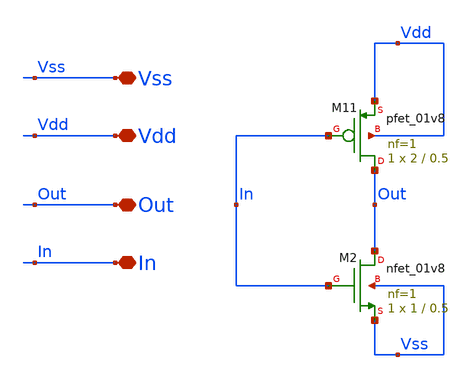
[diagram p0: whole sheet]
** sch_path: xschem/inv_layout_tt.sch
**.subckt inv_layout_tt Vdd Vss In Out
*.iopin Vdd
*.iopin Vss
*.iopin In
*.iopin Out
XM11 Out In Vdd Vdd sky130_fd_pr__pfet_01v8 L=0.5 W=2 nf=1 ad='int((nf+1)/2) * W/nf * 0.29' as='int((nf+2)/2) * W/nf * 0.29'
+ pd='2*int((nf+1)/2) * (W/nf + 0.29)' ps='2*int((nf+2)/2) * (W/nf + 0.29)' nrd='0.29 / W' nrs='0.29 / W'
+ sa=0 sb=0 sd=0 mult=1 m=1
XM2 Out In Vss Vss sky130_fd_pr__nfet_01v8 L=0.5 W=1 nf=1 ad='int((1 + 1)/2) * 1 / 1 * 0.29' as='int((1 + 2)/2) * 1 / 1 * 0.29'
+ pd='2*int((1 + 1)/2) * (1 / 1 + 0.29)' ps='2*int((1 + 2)/2) * (1 / 1 + 0.29)' nrd='0.29 / 1 ' nrs='0.29 / 1 '
+ sa=0 sb=0 sd=0 mult=1 m=1
**.ends
.end
